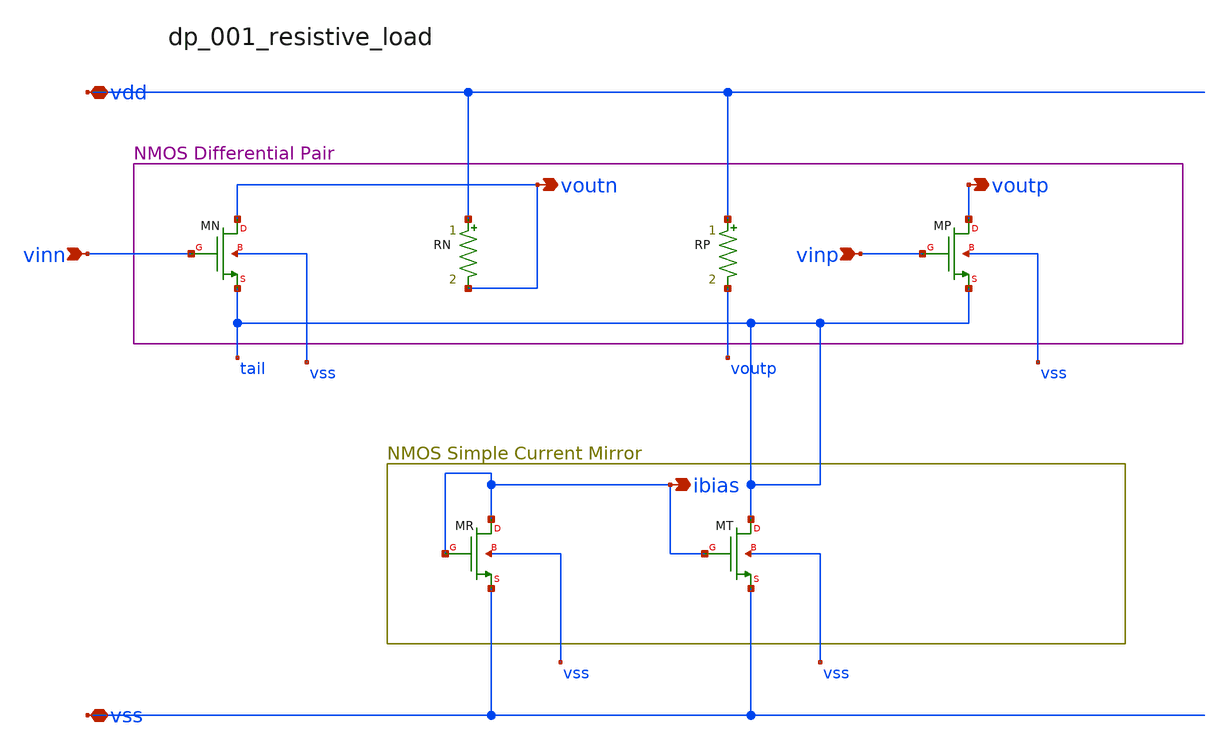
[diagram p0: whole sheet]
** sch_path: analog-db/raw/dp_001_resistive_load/dp_001_resistive_load_annotated.sch
**.subckt dp_001_resistive_load_annotated vinn vinp vdd vss voutn voutp ibias
*.ipin vinn
*.ipin vinp
*.iopin vdd
*.iopin vss
*.opin voutn
*.opin voutp
*.opin ibias
RN vdd voutn x_dut_rn_value m=1
RP vdd voutp x_dut_rp_value m=1
XMN voutn vinn tail vss sg13_lv_nmos w=x_dut_xmn_w l=x_dut_xmn_l ng=1 m=x_dut_xmn_m
XMP voutp vinp tail vss sg13_lv_nmos w=x_dut_xmp_w l=x_dut_xmp_l ng=1 m=x_dut_xmp_m
XMR ibias ibias vss vss sg13_lv_nmos w=x_dut_xmr_w l=x_dut_xmr_l ng=1 m=x_dut_xmr_m
XMT tail ibias vss vss sg13_lv_nmos w=x_dut_xmt_w l=x_dut_xmt_l ng=1 m=x_dut_xmt_m
**.ends
.end
